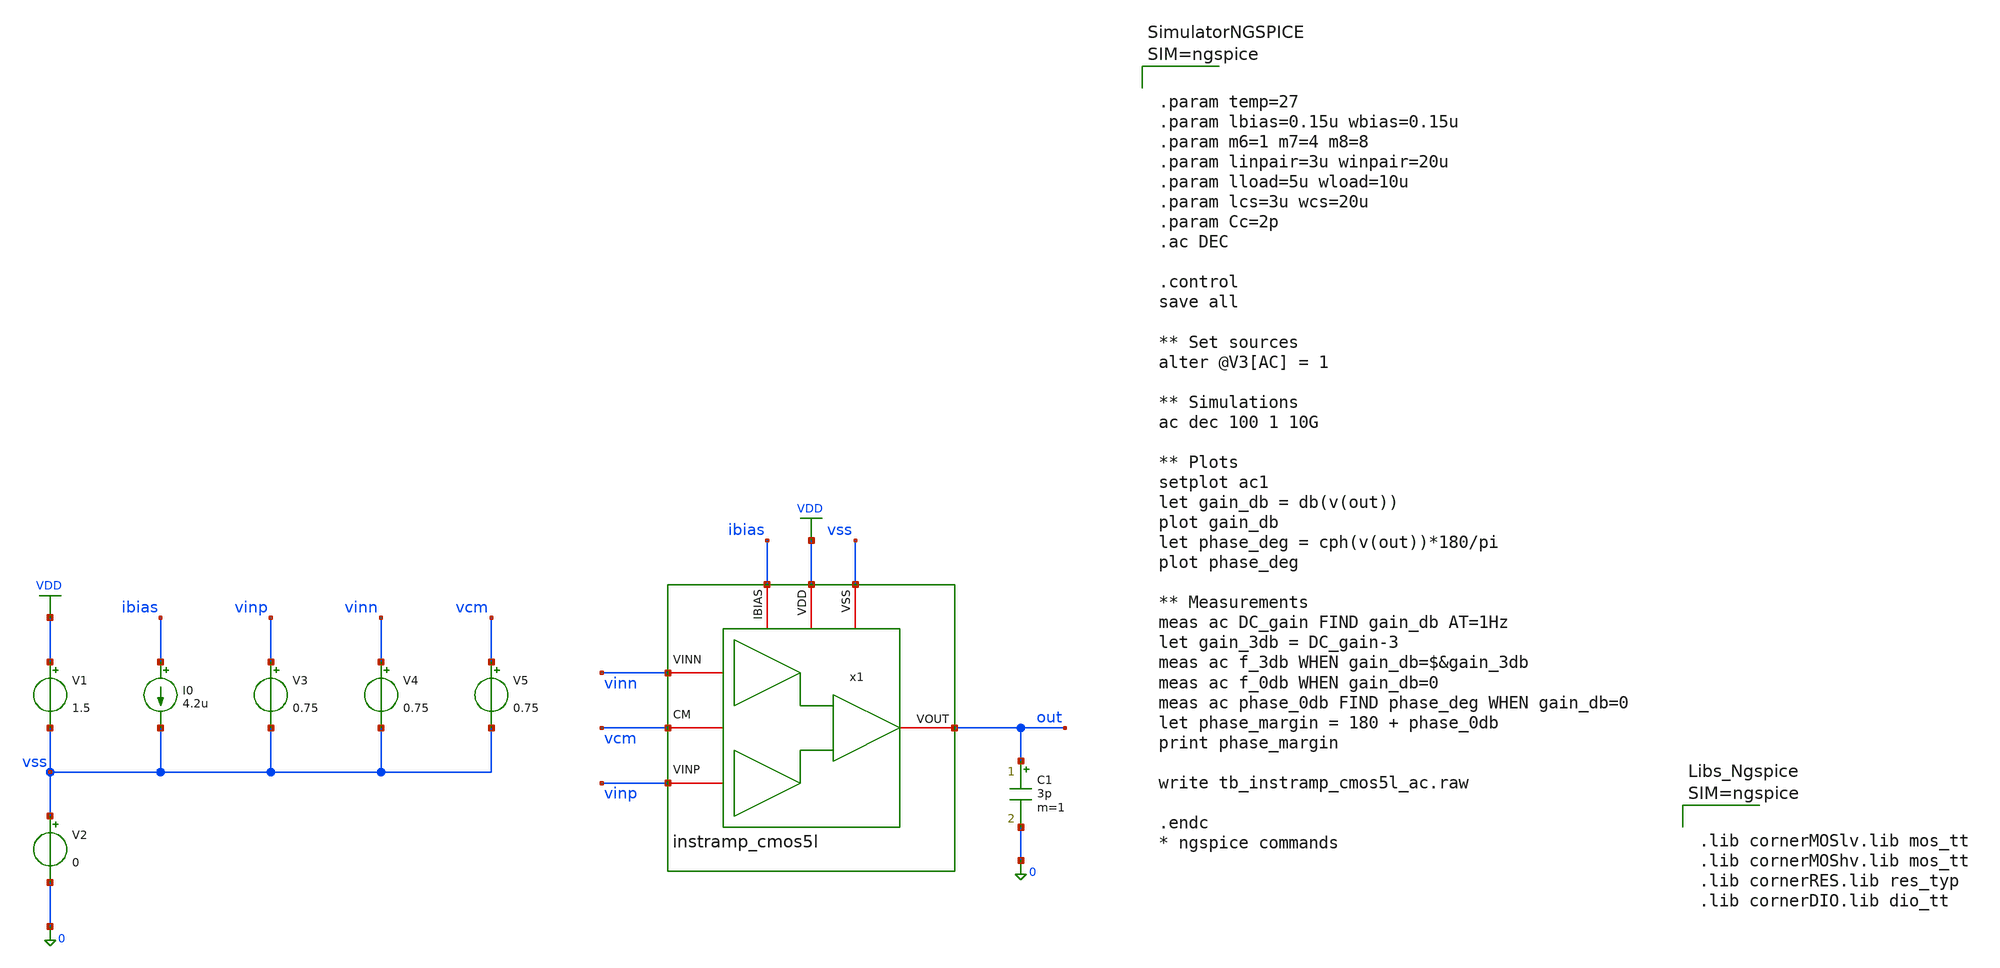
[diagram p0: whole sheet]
** sch_path: xschem/instramp_cmos5l/tb/tb_instramp_cmos5l_ac/tb_instramp_cmos5l_ac.sch
**.subckt tb_instramp_cmos5l_ac
C1 out 0 3p m=1
I0 ibias vss 4.2u
V1 VDD vss 1.5
V2 vss 0 0
V3 vinp vss 0.75
V4 vinn vss 0.75
x1 vss VDD ibias vinn out vinp vcm instramp_cmos5l
V5 vcm vss 0.75
**** begin user architecture code



.param temp=27
.param lbias=0.15u wbias=0.15u
.param m6=1 m7=4 m8=8
.param linpair=3u winpair=20u
.param lload=5u wload=10u
.param lcs=3u wcs=20u
.param Cc=2p
.ac DEC

.control
save all

** Set sources
alter @V3[AC] = 1

** Simulations
ac dec 100 1 10G

** Plots
setplot ac1
let gain_db = db(v(out))
plot gain_db
let phase_deg = cph(v(out))*180/pi
plot phase_deg

** Measurements
meas ac DC_gain FIND gain_db AT=1Hz
let gain_3db = DC_gain-3
meas ac f_3db WHEN gain_db=$&gain_3db
meas ac f_0db WHEN gain_db=0
meas ac phase_0db FIND phase_deg WHEN gain_db=0
let phase_margin = 180 + phase_0db
print phase_margin

write tb_instramp_cmos5l_ac.raw

.endc
* ngspice commands






.lib cornerMOSlv.lib mos_tt
.lib cornerMOShv.lib mos_tt
.lib cornerRES.lib res_typ
.lib cornerDIO.lib dio_tt



**** end user architecture code
**.ends

* expanding   symbol:
*+  /foss/designs/sg13cmos5l_spma_ip__instramp/xschem/instramp_cmos5l/instramp_cmos5l.sym # of pins=7
** sym_path: /foss/designs/sg13cmos5l_spma_ip__instramp/xschem/instramp_cmos5l/instramp_cmos5l.sym
** sch_path: /foss/designs/sg13cmos5l_spma_ip__instramp/xschem/instramp_cmos5l/instramp_cmos5l.sch
.subckt instramp_cmos5l VSS VDD IBIAS VINN VOUT VINP CM
*.iopin VDD
*.iopin IBIAS
*.iopin VSS
*.iopin CM
*.iopin VOUT
*.iopin VINN
*.iopin VINP
x1 vss ibias vdd net3 VINP net4 ota_cmos5l
x2 vss ibias vdd net1 VINN net2 ota_cmos5l
x3 vss ibias vdd net5 net6 net8 ota_cmos5l
XR1 net4 net6 sub! rhigh w=0.5e-6 l=2e-6 m=1 b=0 mm_ok=1
XR2 net2 net5 sub! rhigh w=0.5e-6 l=2e-6 m=1 b=0 mm_ok=1
XR3 net6 CM sub! rhigh w=0.5e-6 l=8*2.23e-6 m=1 b=0 mm_ok=1
XR4 net5 net7 sub! rhigh w=0.5e-6 l=8*2.23e-6 m=1 b=0 mm_ok=1
Vmeas net7 net8 0
.save i(vmeas)
Vmeas1 net8 VOUT 0
.save i(vmeas1)
R5 VINN vcm 10MEG m=1
R6 vcm VINP 10MEG m=1
XR7 net2 net1 sub! rhigh w=0.5e-6 l=2e-6 m=1 b=0 mm_ok=1
XR8 net4 net3 sub! rhigh w=0.5e-6 l=2e-6 m=1 b=0 mm_ok=1
.ends


* expanding   symbol:  /foss/designs/sg13cmos5l_spma_ip__instramp/xschem/ota_cmos5l/ota_cmos5l.sym #
*+ of pins=6
** sym_path: xschem/output_buffer/ota_cmos5l.sym
** sch_path: xschem/output_buffer/ota_cmos5l.sch
.subckt ota_cmos5l VSS IBIAS VDD VINN VINP VOUT
*.iopin IBIAS
*.iopin VDD
*.iopin VSS
*.iopin VOUT
*.iopin VINP
*.iopin VINN
XM6 IBIAS IBIAS VDD VDD sg13_lv_pmos w={wbias} l={lbias} ng=1 m={m6} mm_ok=1
XM7 net1 IBIAS VDD VDD sg13_lv_pmos w={wbias} l={lbias} ng=1 m={m7} mm_ok=1
XM8 VOUT IBIAS VDD VDD sg13_lv_pmos w={wbias} l={lbias} ng=1 m={m8} mm_ok=1
XM1 net2 VINN net1 VDD sg13_lv_pmos w={winpair} l={linpair} ng=1 m=1 mm_ok=1
XM2 net3 VINP net1 VDD sg13_lv_pmos w={winpair} l={linpair} ng=1 m=1 mm_ok=1
XM3 net2 net2 VSS VSS sg13_lv_nmos w={wload} l={lload} ng=1 m=1 mm_ok=1
XM4 net3 net2 VSS VSS sg13_lv_nmos w={wload} l={lload} ng=1 m=1 mm_ok=1
XM5 VOUT net3 VSS VSS sg13_lv_nmos w={wcs} l={lcs} ng=1 m=1 mm_ok=1
XR1 net3 net4 VSS rhigh w=0.5e-6 l=1.95e-6 m=1 b=0 mm_ok=1
.save v(vinp)
.save v(vinn)
.save v(vout)
XC2 VOUT net4 cap_cmomi w=15e-6 l=15e-6 mmin=1 mmax=4 feed=double subblock=0 m=5 mm_ok=1
**** begin user architecture code


.param temp=27
.param lbias=0.15u wbias=0.15u
.param m6=1 m7=4 m8=8
.param linpair=3u winpair=20u
.param lload=5u wload=10u
.param lcs=3u wcs=20u
.param Cc=2p



**** end user architecture code
XC1 VOUT net4 cap_cmomi w=15e-6 l=15e-6 mmin=1 mmax=4 feed=double subblock=0 m=4 mm_ok=1
.ends

.GLOBAL VDD
.end
